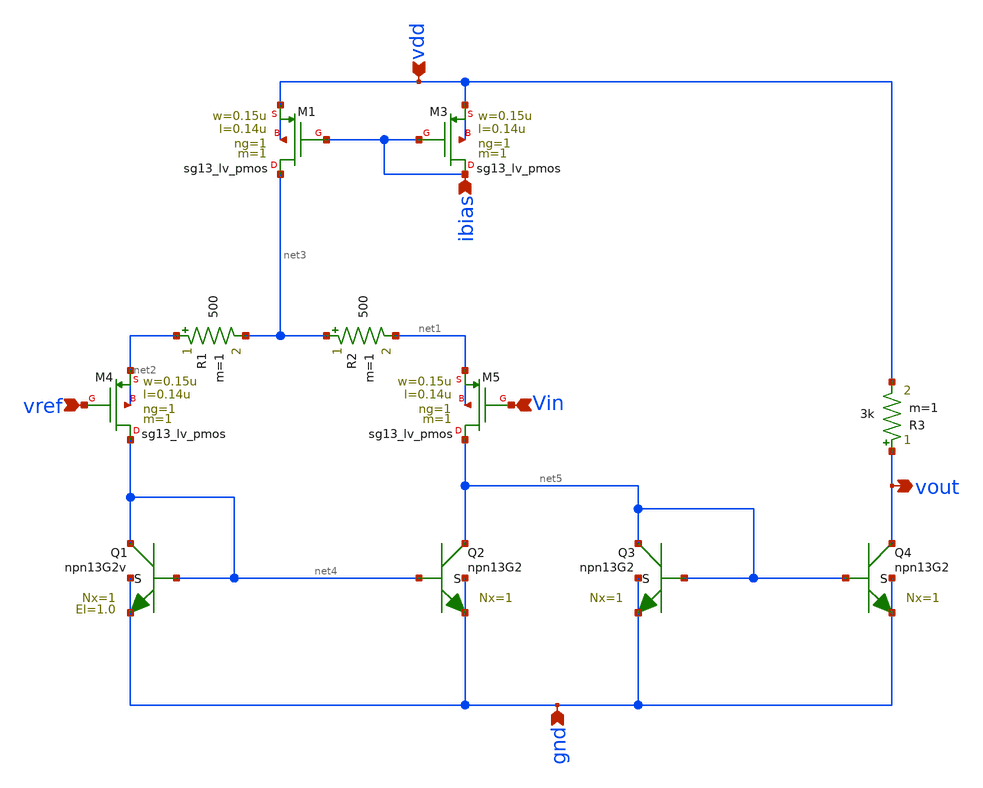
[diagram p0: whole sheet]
** sch_path: spice/decoderCellBJT.sch
**.subckt decoderCellBJT vdd gnd vout ibias Vin vref
*.ipin vdd
*.ipin gnd
*.opin vout
*.ipin ibias
*.ipin Vin
*.ipin vref
XM1 net3 ibias vdd vdd sg13_lv_pmos w=0.15u l=0.14u ng=1 m=1 mm_ok=1
XM3 ibias ibias vdd vdd sg13_lv_pmos w=0.15u l=0.14u ng=1 m=1 mm_ok=1
XM4 net4 vref net2 net2 sg13_lv_pmos w=0.15u l=0.14u ng=1 m=1 mm_ok=1
XM5 net5 Vin net1 net1 sg13_lv_pmos w=0.15u l=0.14u ng=1 m=1 mm_ok=1
R1 net2 net3 500 m=1
R2 net3 net1 500 m=1
R3 vout vdd 3k m=1
XQ1 net4 net4 gnd gnd npn13G2v Nx=1 El=1.0 mm_ok=1
XQ2 net5 net4 gnd gnd npn13G2 Nx=1 mm_ok=1
XQ3 net5 net5 gnd gnd npn13G2 Nx=1 mm_ok=1
XQ4 vout net5 gnd gnd npn13G2 Nx=1 mm_ok=1
**.ends
.end
